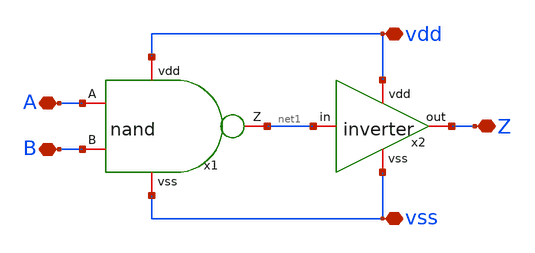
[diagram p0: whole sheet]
** sch_path: designs/sch/and.sch
**.subckt and Z A B vdd vss
*.iopin Z
*.iopin A
*.iopin B
*.iopin vdd
*.iopin vss
x1 vdd net1 A B vss nand
x2 vdd Z net1 vss inverter
**.ends

* expanding   symbol:  /foss/designs/sch/nand.sym # of pins=5
** sym_path: designs/nand.sym
** sch_path: designs/nand.sch
.subckt nand vdd Z A B vss
*.iopin B
*.iopin A
*.iopin vdd
*.iopin Z
*.iopin vss
XM1 net1 B vss vss sky130_fd_pr__nfet_01v8 L=0.15 W=1.5 nf=1 ad='int((nf+1)/2) * W/nf * 0.29' as='int((nf+2)/2) * W/nf * 0.29'
+ pd='2*int((nf+1)/2) * (W/nf + 0.29)' ps='2*int((nf+2)/2) * (W/nf + 0.29)' nrd='0.29 / W' nrs='0.29 / W'
+ sa=0 sb=0 sd=0 mult=1 m=1
XM2 Z A net1 vss sky130_fd_pr__nfet_01v8 L=0.15 W=1.5 nf=1 ad='int((nf+1)/2) * W/nf * 0.29' as='int((nf+2)/2) * W/nf * 0.29'
+ pd='2*int((nf+1)/2) * (W/nf + 0.29)' ps='2*int((nf+2)/2) * (W/nf + 0.29)' nrd='0.29 / W' nrs='0.29 / W'
+ sa=0 sb=0 sd=0 mult=1 m=1
XM3 Z A vdd vdd sky130_fd_pr__pfet_01v8 L=0.15 W=1.5 nf=1 ad='int((nf+1)/2) * W/nf * 0.29' as='int((nf+2)/2) * W/nf * 0.29'
+ pd='2*int((nf+1)/2) * (W/nf + 0.29)' ps='2*int((nf+2)/2) * (W/nf + 0.29)' nrd='0.29 / W' nrs='0.29 / W'
+ sa=0 sb=0 sd=0 mult=1 m=1
XM4 Z B vdd vdd sky130_fd_pr__pfet_01v8 L=0.15 W=1.5 nf=1 ad='int((nf+1)/2) * W/nf * 0.29' as='int((nf+2)/2) * W/nf * 0.29'
+ pd='2*int((nf+1)/2) * (W/nf + 0.29)' ps='2*int((nf+2)/2) * (W/nf + 0.29)' nrd='0.29 / W' nrs='0.29 / W'
+ sa=0 sb=0 sd=0 mult=1 m=1
.ends


* expanding   symbol:  /foss/designs/sch/inverter.sym # of pins=4
** sym_path: designs/inverter.sym
** sch_path: designs/inverter.sch
.subckt inverter vdd out in vss
*.iopin out
*.iopin vss
*.iopin vdd
*.iopin in
XM2 out in vss vss sky130_fd_pr__nfet_01v8 L=0.15 W=0.75 nf=1 ad='int((nf+1)/2) * W/nf * 0.29' as='int((nf+2)/2) * W/nf * 0.29'
+ pd='2*int((nf+1)/2) * (W/nf + 0.29)' ps='2*int((nf+2)/2) * (W/nf + 0.29)' nrd='0.29 / W' nrs='0.29 / W'
+ sa=0 sb=0 sd=0 mult=1 m=1
XM1 out in vdd vdd sky130_fd_pr__pfet_01v8 L=0.15 W=1.5 nf=1 ad='int((nf+1)/2) * W/nf * 0.29' as='int((nf+2)/2) * W/nf * 0.29'
+ pd='2*int((nf+1)/2) * (W/nf + 0.29)' ps='2*int((nf+2)/2) * (W/nf + 0.29)' nrd='0.29 / W' nrs='0.29 / W'
+ sa=0 sb=0 sd=0 mult=1 m=1
.ends

.end
